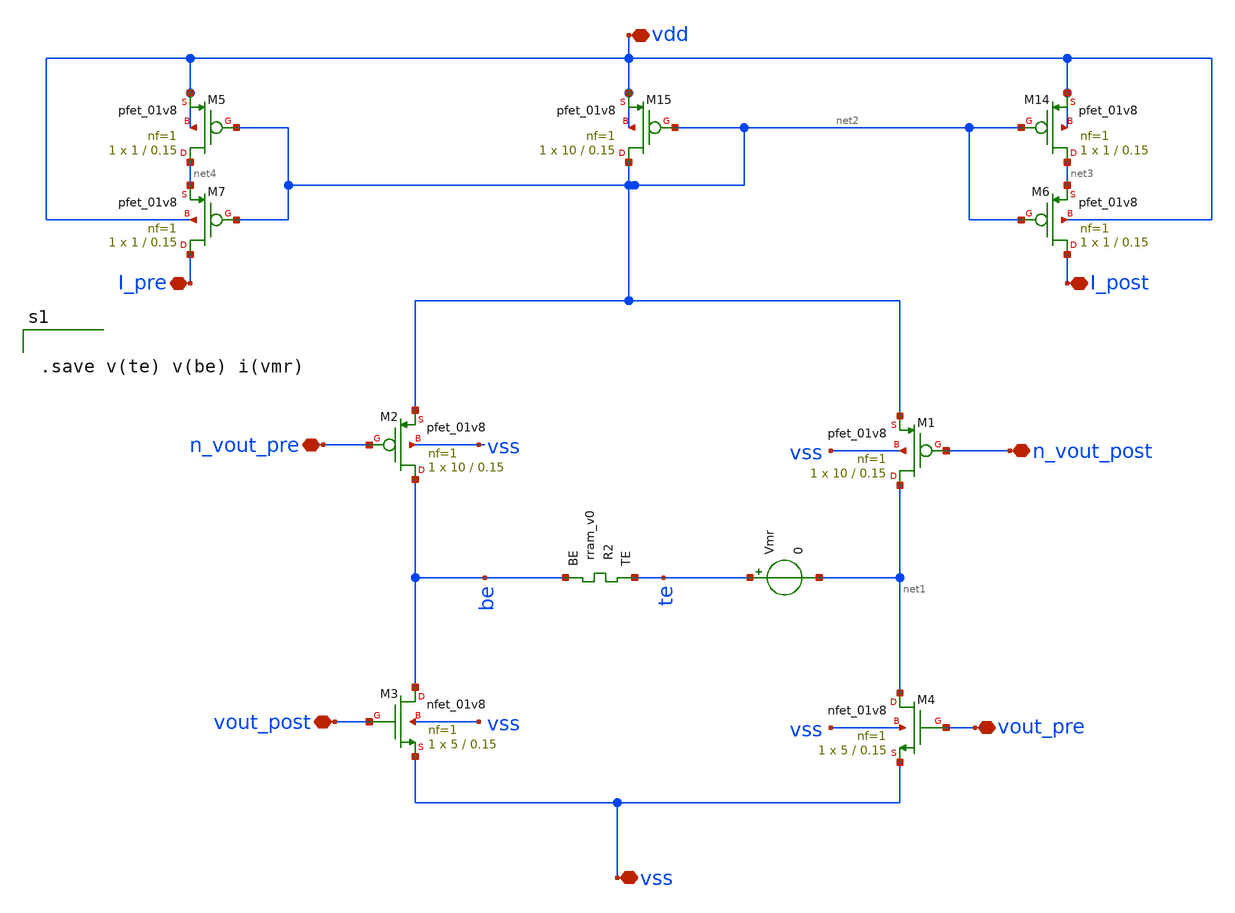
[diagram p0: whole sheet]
** sch_path: Synapse/stdp_bp.sch
**.subckt stdp_bp vdd vss vout_post vout_pre I_post n_vout_pre n_vout_post I_pre
*.iopin vdd
*.iopin vss
*.iopin vout_post
*.iopin vout_pre
*.iopin I_post
*.iopin n_vout_pre
*.iopin n_vout_post
*.iopin I_pre
XM3 be vout_post vss vss sky130_fd_pr__nfet_01v8 L=0.15 W=5 nf=1 ad='int((nf+1)/2) * W/nf * 0.29' as='int((nf+2)/2) * W/nf * 0.29'
+ pd='2*int((nf+1)/2) * (W/nf + 0.29)' ps='2*int((nf+2)/2) * (W/nf + 0.29)' nrd='0.29 / W' nrs='0.29 / W'
+ sa=0 sb=0 sd=0 mult=1 m=1
XM4 net1 vout_pre vss vss sky130_fd_pr__nfet_01v8 L=0.15 W=5 nf=1 ad='int((nf+1)/2) * W/nf * 0.29' as='int((nf+2)/2) * W/nf * 0.29'
+ pd='2*int((nf+1)/2) * (W/nf + 0.29)' ps='2*int((nf+2)/2) * (W/nf + 0.29)' nrd='0.29 / W' nrs='0.29 / W'
+ sa=0 sb=0 sd=0 mult=1 m=1
XR2 te be rram_v0
XM14 net3 net2 vdd vdd sky130_fd_pr__pfet_01v8 L=0.15 W=1 nf=1 ad='int((nf+1)/2) * W/nf * 0.29' as='int((nf+2)/2) * W/nf * 0.29'
+ pd='2*int((nf+1)/2) * (W/nf + 0.29)' ps='2*int((nf+2)/2) * (W/nf + 0.29)' nrd='0.29 / W' nrs='0.29 / W'
+ sa=0 sb=0 sd=0 mult=1 m=1
XM15 net2 net2 vdd vdd sky130_fd_pr__pfet_01v8 L=0.15 W=10 nf=1 ad='int((nf+1)/2) * W/nf * 0.29' as='int((nf+2)/2) * W/nf * 0.29'
+ pd='2*int((nf+1)/2) * (W/nf + 0.29)' ps='2*int((nf+2)/2) * (W/nf + 0.29)' nrd='0.29 / W' nrs='0.29 / W'
+ sa=0 sb=0 sd=0 mult=1 m=1
Vmr te net1 0
.save i(vmr)
XM1 net1 n_vout_post net2 vss sky130_fd_pr__pfet_01v8 L=0.15 W=10 nf=1 ad='int((nf+1)/2) * W/nf * 0.29'
+ as='int((nf+2)/2) * W/nf * 0.29' pd='2*int((nf+1)/2) * (W/nf + 0.29)' ps='2*int((nf+2)/2) * (W/nf + 0.29)'
+ nrd='0.29 / W' nrs='0.29 / W' sa=0 sb=0 sd=0 mult=1 m=1
XM2 be n_vout_pre net2 vss sky130_fd_pr__pfet_01v8 L=0.15 W=10 nf=1 ad='int((nf+1)/2) * W/nf * 0.29'
+ as='int((nf+2)/2) * W/nf * 0.29' pd='2*int((nf+1)/2) * (W/nf + 0.29)' ps='2*int((nf+2)/2) * (W/nf + 0.29)'
+ nrd='0.29 / W' nrs='0.29 / W' sa=0 sb=0 sd=0 mult=1 m=1
XM6 I_post net2 net3 vdd sky130_fd_pr__pfet_01v8 L=0.15 W=1 nf=1 ad='int((nf+1)/2) * W/nf * 0.29' as='int((nf+2)/2) * W/nf * 0.29'
+ pd='2*int((nf+1)/2) * (W/nf + 0.29)' ps='2*int((nf+2)/2) * (W/nf + 0.29)' nrd='0.29 / W' nrs='0.29 / W'
+ sa=0 sb=0 sd=0 mult=1 m=1
XM5 net4 net2 vdd vdd sky130_fd_pr__pfet_01v8 L=0.15 W=1 nf=1 ad='int((nf+1)/2) * W/nf * 0.29' as='int((nf+2)/2) * W/nf * 0.29'
+ pd='2*int((nf+1)/2) * (W/nf + 0.29)' ps='2*int((nf+2)/2) * (W/nf + 0.29)' nrd='0.29 / W' nrs='0.29 / W'
+ sa=0 sb=0 sd=0 mult=1 m=1
XM7 I_pre net2 net4 vdd sky130_fd_pr__pfet_01v8 L=0.15 W=1 nf=1 ad='int((nf+1)/2) * W/nf * 0.29' as='int((nf+2)/2) * W/nf * 0.29'
+ pd='2*int((nf+1)/2) * (W/nf + 0.29)' ps='2*int((nf+2)/2) * (W/nf + 0.29)' nrd='0.29 / W' nrs='0.29 / W'
+ sa=0 sb=0 sd=0 mult=1 m=1
**** begin user architecture code


.save v(te) v(be) i(vmr)


**** end user architecture code
**.ends
.end
